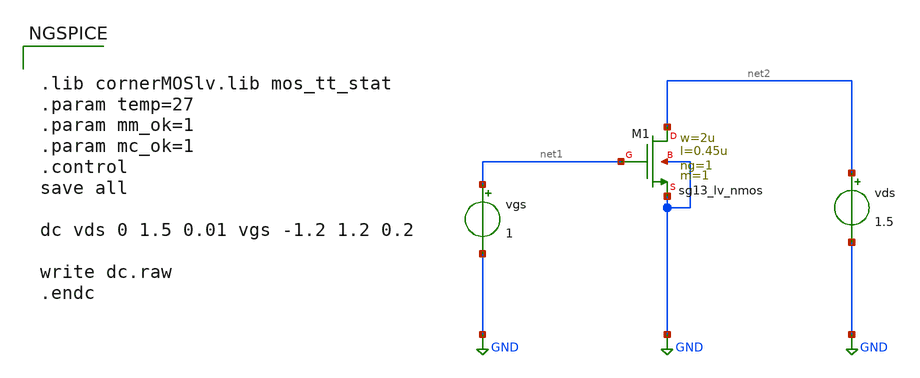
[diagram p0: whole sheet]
** sch_path: lectures/2025-08-28/dc.sch
**.subckt dc
XM1 net2 net1 GND GND sg13_lv_nmos w=2u l=0.45u ng=1 m=1 mm_ok=1
vgs net1 GND 1
.save i(vgs)
vds net2 GND 1.5
.save i(vds)
**** begin user architecture code


.lib cornerMOSlv.lib mos_tt_stat
.param temp=27
.param mm_ok=1
.param mc_ok=1
.control
save all

dc vds 0 1.5 0.01 vgs -1.2 1.2 0.2

write dc.raw
.endc


**** end user architecture code
**.ends
.GLOBAL GND
.end
